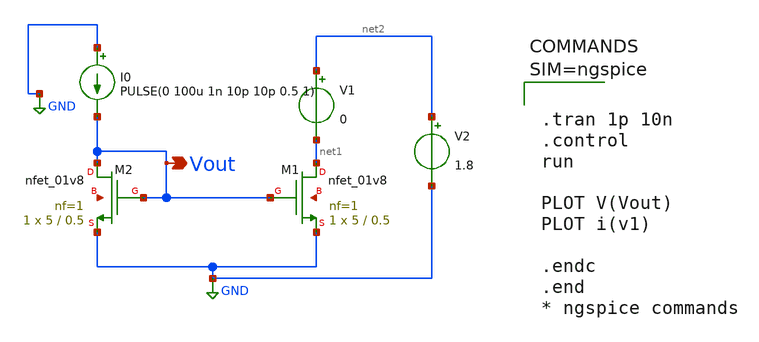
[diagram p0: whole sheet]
** sch_path: spice/current_m_trans.sch
**.subckt current_m_trans Vout
*.opin Vout
XM2 Vout Vout GND net3 sky130_fd_pr__nfet_01v8 L=0.5 W=5 nf=1 ad='int((1 + 1)/2) * 5 / 1 * 0.29' as='int((1 + 2)/2) * 5 / 1 * 0.29'
+ pd='2*int((1 + 1)/2) * (5 / 1 + 0.29)' ps='2*int((1 + 2)/2) * (5 / 1 + 0.29)' nrd='0.29 / 5 ' nrs='0.29 / 5 '
+ sa=0 sb=0 sd=0 mult=1 m=1
XM1 net1 Vout GND net4 sky130_fd_pr__nfet_01v8 L=0.5 W=5 nf=1 ad='int((1 + 1)/2) * 5 / 1 * 0.29' as='int((1 + 2)/2) * 5 / 1 * 0.29'
+ pd='2*int((1 + 1)/2) * (5 / 1 + 0.29)' ps='2*int((1 + 2)/2) * (5 / 1 + 0.29)' nrd='0.29 / 5 ' nrs='0.29 / 5 '
+ sa=0 sb=0 sd=0 mult=1 m=1
I0 GND Vout PULSE(0 100u 1n 10p 10p 0.5 1)
V1 net2 net1 0
V2 net2 GND 1.8
**** begin user architecture code

** opencircuitdesign pdks install
.lib $::SKYWATER_MODELS/sky130.lib.spice tt




.tran 1p 10n
.control
run

PLOT V(Vout)
PLOT i(v1)

.endc
.end
* ngspice commands



**** end user architecture code
**.ends
.GLOBAL GND
.end
